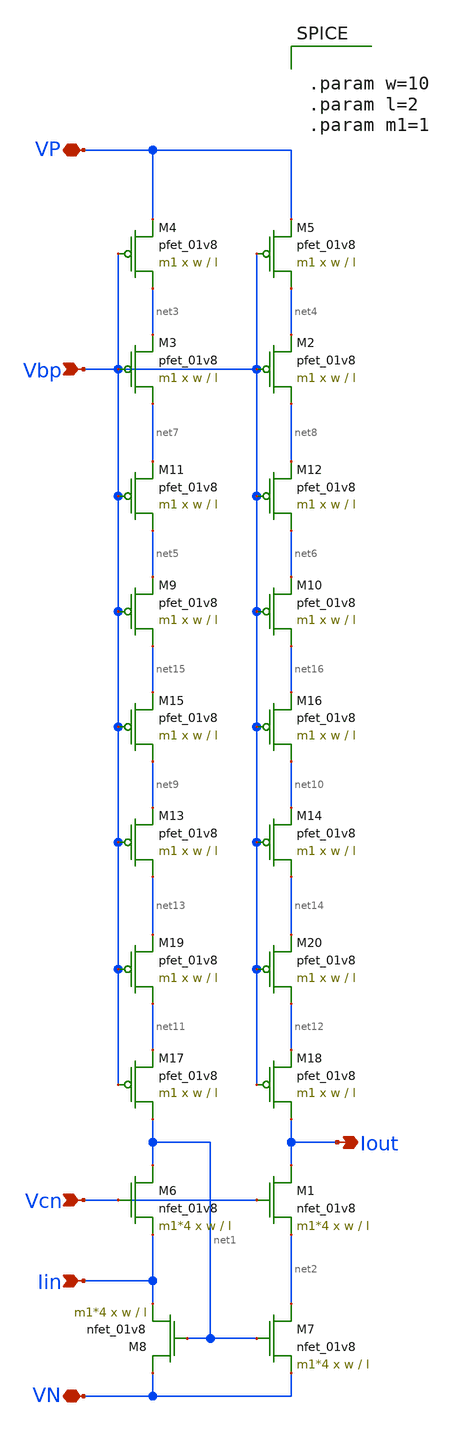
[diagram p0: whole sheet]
** sch_path: schematic/old/iout_mirror.sch
**.subckt iout_mirror Vbp VN Iin Vcn VP Iout
*.ipin Vbp
*.iopin VN
*.ipin Iin
*.ipin Vcn
*.iopin VP
*.opin Iout
XM3 net7 Vbp net3 VDD sky130_fd_pr__pfet_01v8 L=l W=w nf=1 ad='int((nf+1)/2) * W/nf * 0.29' as='int((nf+2)/2) * W/nf * 0.29'
+ pd='2*int((nf+1)/2) * (W/nf + 0.29)' ps='2*int((nf+2)/2) * (W/nf + 0.29)' nrd='0.29 / W' nrs='0.29 / W'
+ sa=0 sb=0 sd=0 mult=m1 m=m1
XM6 net1 Vcn Iin GND sky130_fd_pr__nfet_01v8 L=l W=w nf=1 ad='int((nf+1)/2) * W/nf * 0.29' as='int((nf+2)/2) * W/nf * 0.29'
+ pd='2*int((nf+1)/2) * (W/nf + 0.29)' ps='2*int((nf+2)/2) * (W/nf + 0.29)' nrd='0.29 / W' nrs='0.29 / W'
+ sa=0 sb=0 sd=0 mult=m1*4 m=m1*4
XM2 net8 Vbp net4 VDD sky130_fd_pr__pfet_01v8 L=l W=w nf=1 ad='int((nf+1)/2) * W/nf * 0.29' as='int((nf+2)/2) * W/nf * 0.29'
+ pd='2*int((nf+1)/2) * (W/nf + 0.29)' ps='2*int((nf+2)/2) * (W/nf + 0.29)' nrd='0.29 / W' nrs='0.29 / W'
+ sa=0 sb=0 sd=0 mult=m1 m=m1
XM1 Iout Vcn net2 GND sky130_fd_pr__nfet_01v8 L=l W=w nf=1 ad='int((nf+1)/2) * W/nf * 0.29' as='int((nf+2)/2) * W/nf * 0.29'
+ pd='2*int((nf+1)/2) * (W/nf + 0.29)' ps='2*int((nf+2)/2) * (W/nf + 0.29)' nrd='0.29 / W' nrs='0.29 / W'
+ sa=0 sb=0 sd=0 mult=m1*4 m=m1*4
XM7 net2 net1 VN GND sky130_fd_pr__nfet_01v8 L=l W=w nf=1 ad='int((nf+1)/2) * W/nf * 0.29' as='int((nf+2)/2) * W/nf * 0.29'
+ pd='2*int((nf+1)/2) * (W/nf + 0.29)' ps='2*int((nf+2)/2) * (W/nf + 0.29)' nrd='0.29 / W' nrs='0.29 / W'
+ sa=0 sb=0 sd=0 mult=m1*4 m=m1*4
XM8 VN net1 Iin GND sky130_fd_pr__nfet_01v8 L=l W=w nf=1 ad='int((nf+1)/2) * W/nf * 0.29' as='int((nf+2)/2) * W/nf * 0.29'
+ pd='2*int((nf+1)/2) * (W/nf + 0.29)' ps='2*int((nf+2)/2) * (W/nf + 0.29)' nrd='0.29 / W' nrs='0.29 / W'
+ sa=0 sb=0 sd=0 mult=m1*4 m=m1*4
XM4 net3 Vbp VP VDD sky130_fd_pr__pfet_01v8 L=l W=w nf=1 ad='int((nf+1)/2) * W/nf * 0.29' as='int((nf+2)/2) * W/nf * 0.29'
+ pd='2*int((nf+1)/2) * (W/nf + 0.29)' ps='2*int((nf+2)/2) * (W/nf + 0.29)' nrd='0.29 / W' nrs='0.29 / W'
+ sa=0 sb=0 sd=0 mult=m1 m=m1
XM5 net4 Vbp VP VDD sky130_fd_pr__pfet_01v8 L=l W=w nf=1 ad='int((nf+1)/2) * W/nf * 0.29' as='int((nf+2)/2) * W/nf * 0.29'
+ pd='2*int((nf+1)/2) * (W/nf + 0.29)' ps='2*int((nf+2)/2) * (W/nf + 0.29)' nrd='0.29 / W' nrs='0.29 / W'
+ sa=0 sb=0 sd=0 mult=m1 m=m1
XM9 net15 Vbp net5 VDD sky130_fd_pr__pfet_01v8 L=l W=w nf=1 ad='int((nf+1)/2) * W/nf * 0.29' as='int((nf+2)/2) * W/nf * 0.29'
+ pd='2*int((nf+1)/2) * (W/nf + 0.29)' ps='2*int((nf+2)/2) * (W/nf + 0.29)' nrd='0.29 / W' nrs='0.29 / W'
+ sa=0 sb=0 sd=0 mult=m1 m=m1
XM10 net16 Vbp net6 VDD sky130_fd_pr__pfet_01v8 L=l W=w nf=1 ad='int((nf+1)/2) * W/nf * 0.29' as='int((nf+2)/2) * W/nf * 0.29'
+ pd='2*int((nf+1)/2) * (W/nf + 0.29)' ps='2*int((nf+2)/2) * (W/nf + 0.29)' nrd='0.29 / W' nrs='0.29 / W'
+ sa=0 sb=0 sd=0 mult=m1 m=m1
XM11 net5 Vbp net7 VDD sky130_fd_pr__pfet_01v8 L=l W=w nf=1 ad='int((nf+1)/2) * W/nf * 0.29' as='int((nf+2)/2) * W/nf * 0.29'
+ pd='2*int((nf+1)/2) * (W/nf + 0.29)' ps='2*int((nf+2)/2) * (W/nf + 0.29)' nrd='0.29 / W' nrs='0.29 / W'
+ sa=0 sb=0 sd=0 mult=m1 m=m1
XM12 net6 Vbp net8 VDD sky130_fd_pr__pfet_01v8 L=l W=w nf=1 ad='int((nf+1)/2) * W/nf * 0.29' as='int((nf+2)/2) * W/nf * 0.29'
+ pd='2*int((nf+1)/2) * (W/nf + 0.29)' ps='2*int((nf+2)/2) * (W/nf + 0.29)' nrd='0.29 / W' nrs='0.29 / W'
+ sa=0 sb=0 sd=0 mult=m1 m=m1
XM13 net13 Vbp net9 VDD sky130_fd_pr__pfet_01v8 L=l W=w nf=1 ad='int((nf+1)/2) * W/nf * 0.29' as='int((nf+2)/2) * W/nf * 0.29'
+ pd='2*int((nf+1)/2) * (W/nf + 0.29)' ps='2*int((nf+2)/2) * (W/nf + 0.29)' nrd='0.29 / W' nrs='0.29 / W'
+ sa=0 sb=0 sd=0 mult=m1 m=m1
XM14 net14 Vbp net10 VDD sky130_fd_pr__pfet_01v8 L=l W=w nf=1 ad='int((nf+1)/2) * W/nf * 0.29' as='int((nf+2)/2) * W/nf * 0.29'
+ pd='2*int((nf+1)/2) * (W/nf + 0.29)' ps='2*int((nf+2)/2) * (W/nf + 0.29)' nrd='0.29 / W' nrs='0.29 / W'
+ sa=0 sb=0 sd=0 mult=m1 m=m1
XM15 net9 Vbp net15 VDD sky130_fd_pr__pfet_01v8 L=l W=w nf=1 ad='int((nf+1)/2) * W/nf * 0.29' as='int((nf+2)/2) * W/nf * 0.29'
+ pd='2*int((nf+1)/2) * (W/nf + 0.29)' ps='2*int((nf+2)/2) * (W/nf + 0.29)' nrd='0.29 / W' nrs='0.29 / W'
+ sa=0 sb=0 sd=0 mult=m1 m=m1
XM16 net10 Vbp net16 VDD sky130_fd_pr__pfet_01v8 L=l W=w nf=1 ad='int((nf+1)/2) * W/nf * 0.29' as='int((nf+2)/2) * W/nf * 0.29'
+ pd='2*int((nf+1)/2) * (W/nf + 0.29)' ps='2*int((nf+2)/2) * (W/nf + 0.29)' nrd='0.29 / W' nrs='0.29 / W'
+ sa=0 sb=0 sd=0 mult=m1 m=m1
XM17 net1 Vbp net11 VDD sky130_fd_pr__pfet_01v8 L=l W=w nf=1 ad='int((nf+1)/2) * W/nf * 0.29' as='int((nf+2)/2) * W/nf * 0.29'
+ pd='2*int((nf+1)/2) * (W/nf + 0.29)' ps='2*int((nf+2)/2) * (W/nf + 0.29)' nrd='0.29 / W' nrs='0.29 / W'
+ sa=0 sb=0 sd=0 mult=m1 m=m1
XM18 Iout Vbp net12 VDD sky130_fd_pr__pfet_01v8 L=l W=w nf=1 ad='int((nf+1)/2) * W/nf * 0.29' as='int((nf+2)/2) * W/nf * 0.29'
+ pd='2*int((nf+1)/2) * (W/nf + 0.29)' ps='2*int((nf+2)/2) * (W/nf + 0.29)' nrd='0.29 / W' nrs='0.29 / W'
+ sa=0 sb=0 sd=0 mult=m1 m=m1
XM19 net11 Vbp net13 VDD sky130_fd_pr__pfet_01v8 L=l W=w nf=1 ad='int((nf+1)/2) * W/nf * 0.29' as='int((nf+2)/2) * W/nf * 0.29'
+ pd='2*int((nf+1)/2) * (W/nf + 0.29)' ps='2*int((nf+2)/2) * (W/nf + 0.29)' nrd='0.29 / W' nrs='0.29 / W'
+ sa=0 sb=0 sd=0 mult=m1 m=m1
XM20 net12 Vbp net14 VDD sky130_fd_pr__pfet_01v8 L=l W=w nf=1 ad='int((nf+1)/2) * W/nf * 0.29' as='int((nf+2)/2) * W/nf * 0.29'
+ pd='2*int((nf+1)/2) * (W/nf + 0.29)' ps='2*int((nf+2)/2) * (W/nf + 0.29)' nrd='0.29 / W' nrs='0.29 / W'
+ sa=0 sb=0 sd=0 mult=m1 m=m1
**** begin user architecture code


.param w=10
.param l=2
.param m1=1


**** end user architecture code
**.ends
.end
